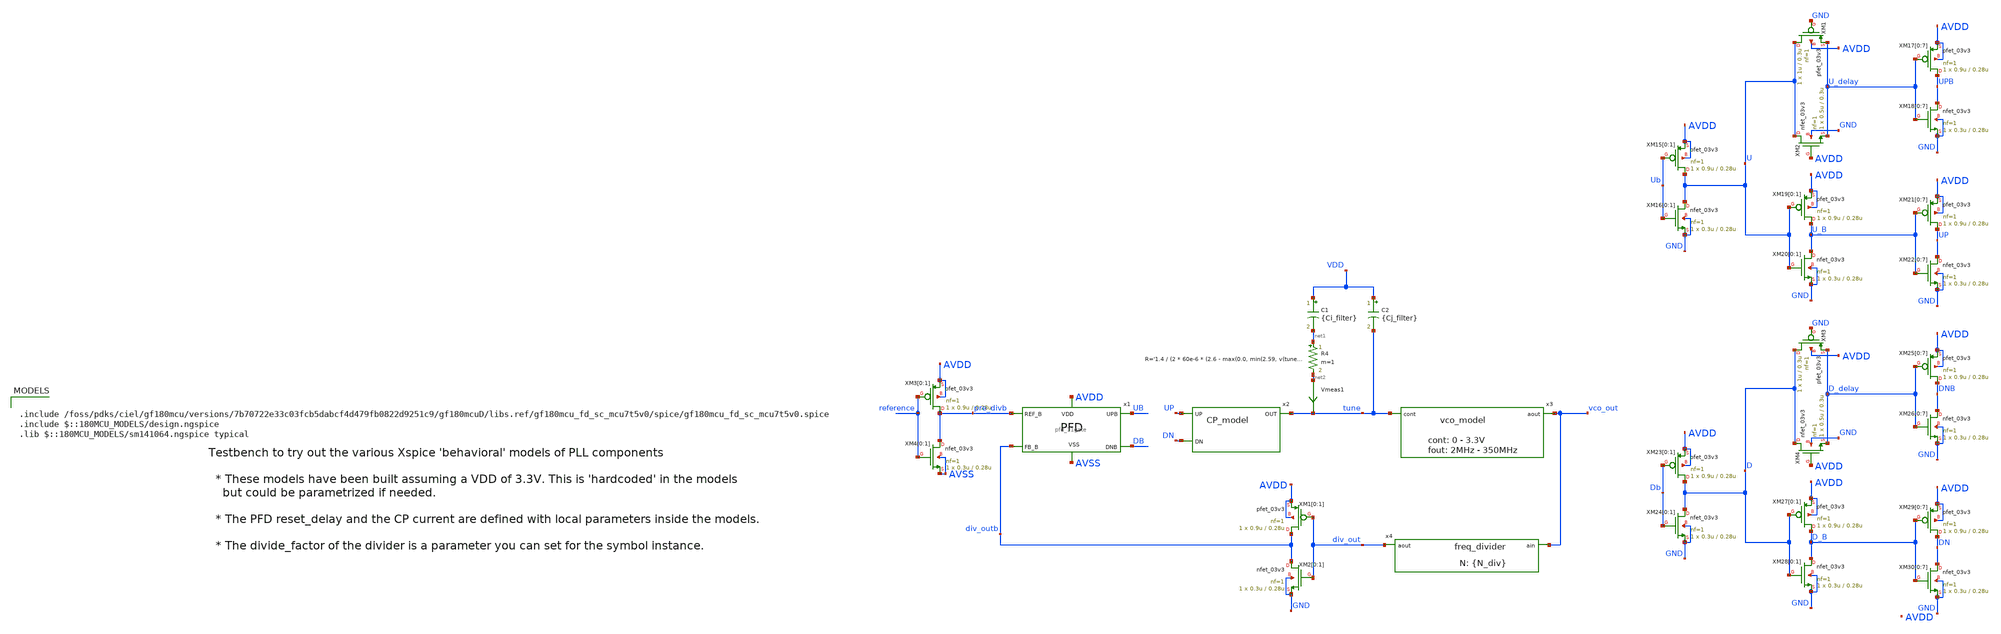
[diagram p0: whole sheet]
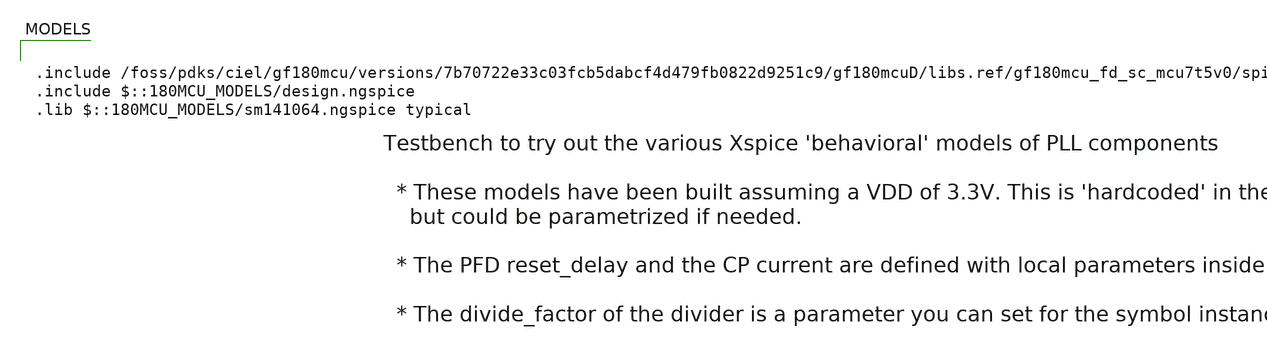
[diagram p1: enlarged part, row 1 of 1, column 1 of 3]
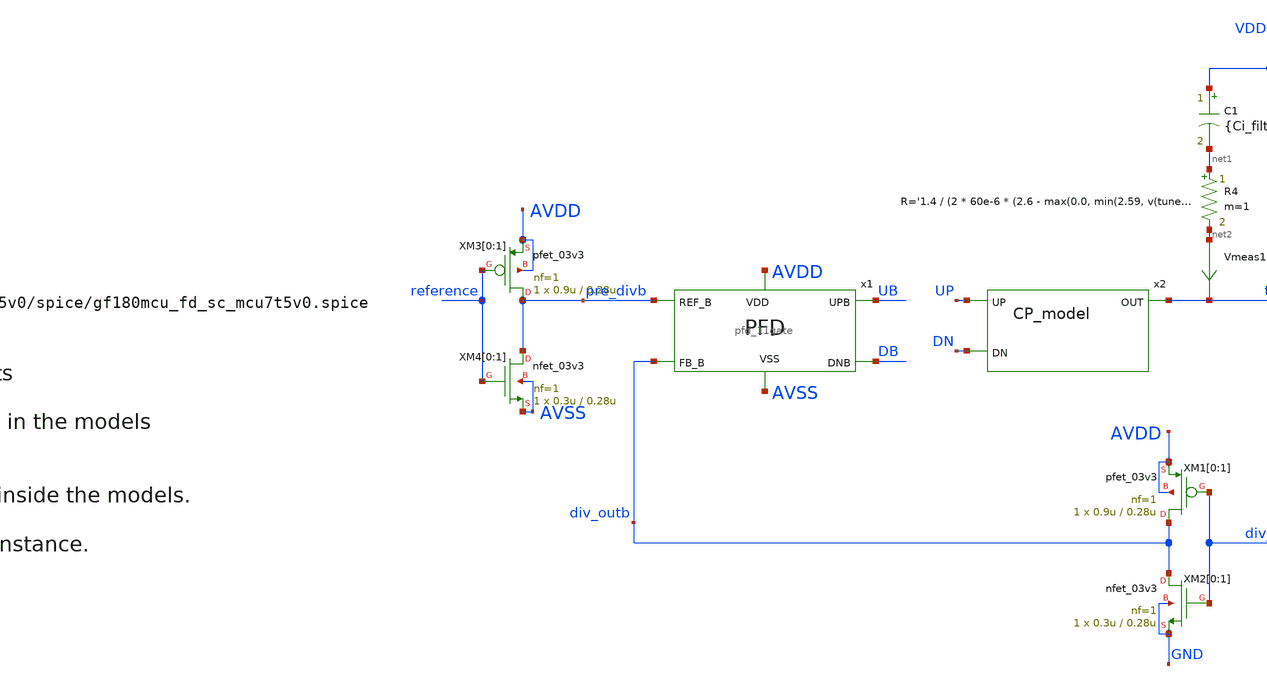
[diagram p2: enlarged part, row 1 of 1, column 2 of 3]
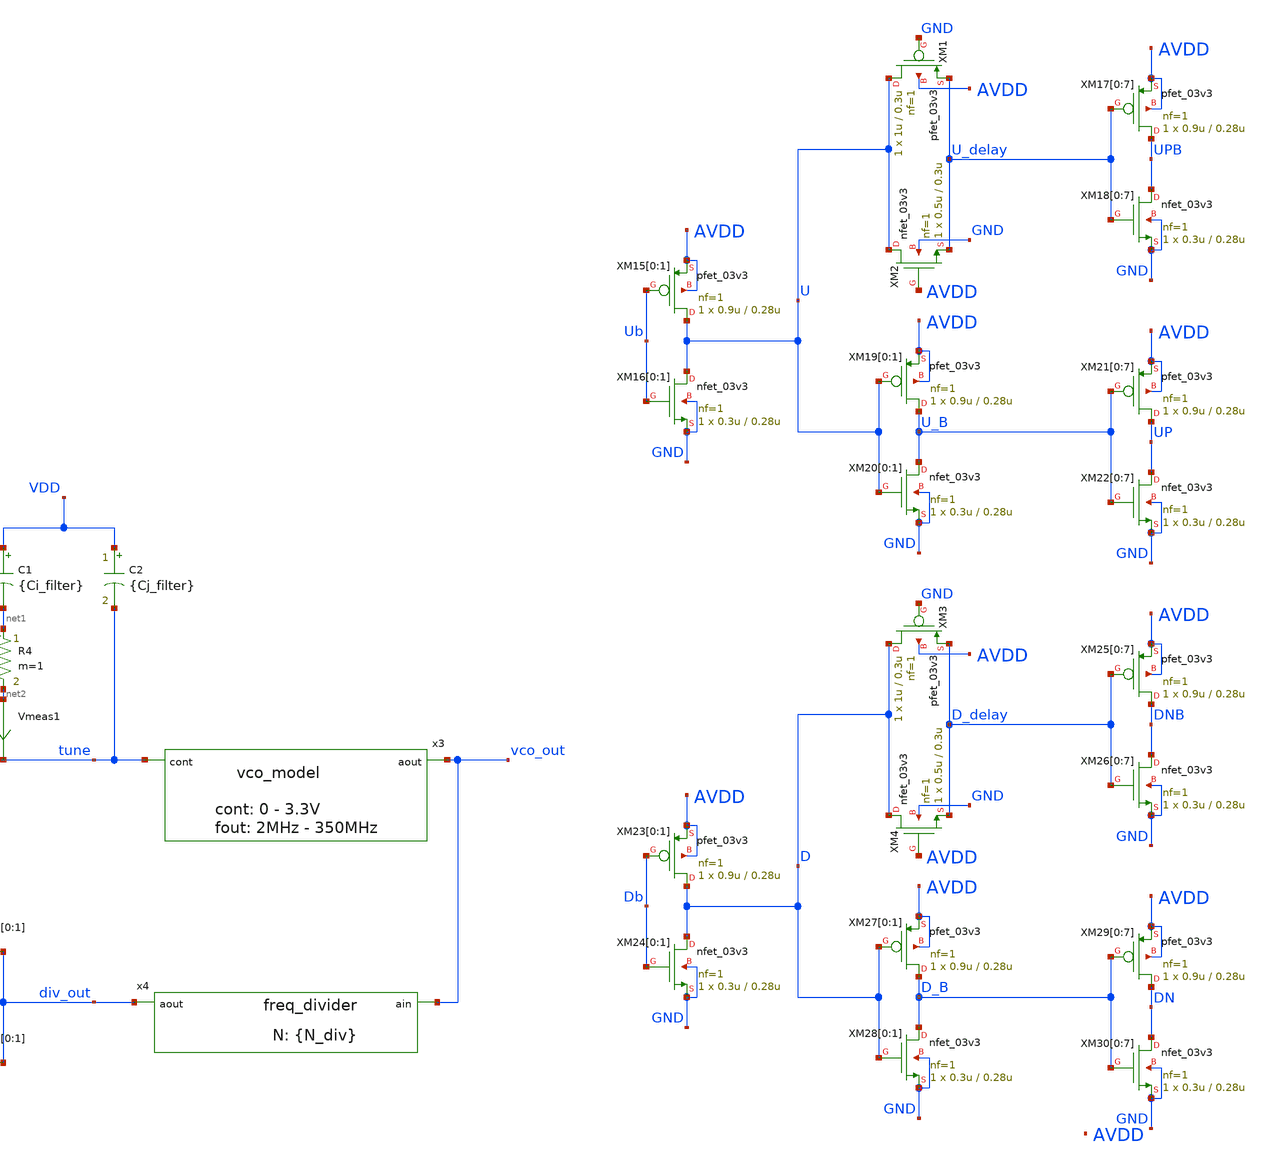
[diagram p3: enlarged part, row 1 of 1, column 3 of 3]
** sch_path: designs/libs/tb_pll/tb_PLL_PFD_model.sch
**.subckt tb_PLL_PFD_model
C1 VDD net1 {Ci_filter} m=1
R4 net1 net2 R='1.4 / (2 * 60e-6 * (2.6 - max(0.0, min(2.59, v(tune)))))' m=1
C2 VDD tune {Cj_filter} m=1
x2 tune UP DN CP_model
x3 vco_out tune vco_model
x4 div_out vco_out freq_divider divide_factor={N_div}
Vmeas1 net2 tune 0
.save i(vmeas1)
x1 pre_divb UB DB div_outb AVDD AVSS pfd_11gate
XM15[0] U Ub AVDD AVDD pfet_03v3 L=0.28u W=0.9u nf=1 ad='int((nf+1)/2) * W/nf * 0.18u' as='int((nf+2)/2) * W/nf * 0.18u'
+ pd='2*int((nf+1)/2) * (W/nf + 0.18u)' ps='2*int((nf+2)/2) * (W/nf + 0.18u)' nrd='0.18u / W' nrs='0.18u / W'
+ sa=0 sb=0 sd=0 m=1
XM15[1] U Ub AVDD AVDD pfet_03v3 L=0.28u W=0.9u nf=1 ad='int((nf+1)/2) * W/nf * 0.18u' as='int((nf+2)/2) * W/nf * 0.18u'
+ pd='2*int((nf+1)/2) * (W/nf + 0.18u)' ps='2*int((nf+2)/2) * (W/nf + 0.18u)' nrd='0.18u / W' nrs='0.18u / W'
+ sa=0 sb=0 sd=0 m=1
XM16[0] U Ub GND GND nfet_03v3 L=0.28u W=0.3u nf=1 ad='int((nf+1)/2) * W/nf * 0.18u' as='int((nf+2)/2) * W/nf * 0.18u'
+ pd='2*int((nf+1)/2) * (W/nf + 0.18u)' ps='2*int((nf+2)/2) * (W/nf + 0.18u)' nrd='0.18u / W' nrs='0.18u / W'
+ sa=0 sb=0 sd=0 m=1
XM16[1] U Ub GND GND nfet_03v3 L=0.28u W=0.3u nf=1 ad='int((nf+1)/2) * W/nf * 0.18u' as='int((nf+2)/2) * W/nf * 0.18u'
+ pd='2*int((nf+1)/2) * (W/nf + 0.18u)' ps='2*int((nf+2)/2) * (W/nf + 0.18u)' nrd='0.18u / W' nrs='0.18u / W'
+ sa=0 sb=0 sd=0 m=1
XM1 U GND U_delay AVDD pfet_03v3 L=0.3u W=1u nf=1 ad='int((nf+1)/2) * W/nf * 0.18u' as='int((nf+2)/2) * W/nf * 0.18u'
+ pd='2*int((nf+1)/2) * (W/nf + 0.18u)' ps='2*int((nf+2)/2) * (W/nf + 0.18u)' nrd='0.18u / W' nrs='0.18u / W'
+ sa=0 sb=0 sd=0 m=1
XM2 U AVDD U_delay GND nfet_03v3 L=0.3u W=0.5u nf=1 ad='int((nf+1)/2) * W/nf * 0.18u' as='int((nf+2)/2) * W/nf * 0.18u'
+ pd='2*int((nf+1)/2) * (W/nf + 0.18u)' ps='2*int((nf+2)/2) * (W/nf + 0.18u)' nrd='0.18u / W' nrs='0.18u / W'
+ sa=0 sb=0 sd=0 m=1
XM17[0] UPB U_delay AVDD AVDD pfet_03v3 L=0.28u W=0.9u nf=1 ad='int((nf+1)/2) * W/nf * 0.18u' as='int((nf+2)/2) * W/nf * 0.18u'
+ pd='2*int((nf+1)/2) * (W/nf + 0.18u)' ps='2*int((nf+2)/2) * (W/nf + 0.18u)' nrd='0.18u / W' nrs='0.18u / W'
+ sa=0 sb=0 sd=0 m=1
XM17[1] UPB U_delay AVDD AVDD pfet_03v3 L=0.28u W=0.9u nf=1 ad='int((nf+1)/2) * W/nf * 0.18u' as='int((nf+2)/2) * W/nf * 0.18u'
+ pd='2*int((nf+1)/2) * (W/nf + 0.18u)' ps='2*int((nf+2)/2) * (W/nf + 0.18u)' nrd='0.18u / W' nrs='0.18u / W'
+ sa=0 sb=0 sd=0 m=1
XM17[2] UPB U_delay AVDD AVDD pfet_03v3 L=0.28u W=0.9u nf=1 ad='int((nf+1)/2) * W/nf * 0.18u' as='int((nf+2)/2) * W/nf * 0.18u'
+ pd='2*int((nf+1)/2) * (W/nf + 0.18u)' ps='2*int((nf+2)/2) * (W/nf + 0.18u)' nrd='0.18u / W' nrs='0.18u / W'
+ sa=0 sb=0 sd=0 m=1
XM17[3] UPB U_delay AVDD AVDD pfet_03v3 L=0.28u W=0.9u nf=1 ad='int((nf+1)/2) * W/nf * 0.18u' as='int((nf+2)/2) * W/nf * 0.18u'
+ pd='2*int((nf+1)/2) * (W/nf + 0.18u)' ps='2*int((nf+2)/2) * (W/nf + 0.18u)' nrd='0.18u / W' nrs='0.18u / W'
+ sa=0 sb=0 sd=0 m=1
XM17[4] UPB U_delay AVDD AVDD pfet_03v3 L=0.28u W=0.9u nf=1 ad='int((nf+1)/2) * W/nf * 0.18u' as='int((nf+2)/2) * W/nf * 0.18u'
+ pd='2*int((nf+1)/2) * (W/nf + 0.18u)' ps='2*int((nf+2)/2) * (W/nf + 0.18u)' nrd='0.18u / W' nrs='0.18u / W'
+ sa=0 sb=0 sd=0 m=1
XM17[5] UPB U_delay AVDD AVDD pfet_03v3 L=0.28u W=0.9u nf=1 ad='int((nf+1)/2) * W/nf * 0.18u' as='int((nf+2)/2) * W/nf * 0.18u'
+ pd='2*int((nf+1)/2) * (W/nf + 0.18u)' ps='2*int((nf+2)/2) * (W/nf + 0.18u)' nrd='0.18u / W' nrs='0.18u / W'
+ sa=0 sb=0 sd=0 m=1
XM17[6] UPB U_delay AVDD AVDD pfet_03v3 L=0.28u W=0.9u nf=1 ad='int((nf+1)/2) * W/nf * 0.18u' as='int((nf+2)/2) * W/nf * 0.18u'
+ pd='2*int((nf+1)/2) * (W/nf + 0.18u)' ps='2*int((nf+2)/2) * (W/nf + 0.18u)' nrd='0.18u / W' nrs='0.18u / W'
+ sa=0 sb=0 sd=0 m=1
XM17[7] UPB U_delay AVDD AVDD pfet_03v3 L=0.28u W=0.9u nf=1 ad='int((nf+1)/2) * W/nf * 0.18u' as='int((nf+2)/2) * W/nf * 0.18u'
+ pd='2*int((nf+1)/2) * (W/nf + 0.18u)' ps='2*int((nf+2)/2) * (W/nf + 0.18u)' nrd='0.18u / W' nrs='0.18u / W'
+ sa=0 sb=0 sd=0 m=1
XM18[0] UPB U_delay GND GND nfet_03v3 L=0.28u W=0.3u nf=1 ad='int((nf+1)/2) * W/nf * 0.18u' as='int((nf+2)/2) * W/nf * 0.18u'
+ pd='2*int((nf+1)/2) * (W/nf + 0.18u)' ps='2*int((nf+2)/2) * (W/nf + 0.18u)' nrd='0.18u / W' nrs='0.18u / W'
+ sa=0 sb=0 sd=0 m=1
XM18[1] UPB U_delay GND GND nfet_03v3 L=0.28u W=0.3u nf=1 ad='int((nf+1)/2) * W/nf * 0.18u' as='int((nf+2)/2) * W/nf * 0.18u'
+ pd='2*int((nf+1)/2) * (W/nf + 0.18u)' ps='2*int((nf+2)/2) * (W/nf + 0.18u)' nrd='0.18u / W' nrs='0.18u / W'
+ sa=0 sb=0 sd=0 m=1
XM18[2] UPB U_delay GND GND nfet_03v3 L=0.28u W=0.3u nf=1 ad='int((nf+1)/2) * W/nf * 0.18u' as='int((nf+2)/2) * W/nf * 0.18u'
+ pd='2*int((nf+1)/2) * (W/nf + 0.18u)' ps='2*int((nf+2)/2) * (W/nf + 0.18u)' nrd='0.18u / W' nrs='0.18u / W'
+ sa=0 sb=0 sd=0 m=1
XM18[3] UPB U_delay GND GND nfet_03v3 L=0.28u W=0.3u nf=1 ad='int((nf+1)/2) * W/nf * 0.18u' as='int((nf+2)/2) * W/nf * 0.18u'
+ pd='2*int((nf+1)/2) * (W/nf + 0.18u)' ps='2*int((nf+2)/2) * (W/nf + 0.18u)' nrd='0.18u / W' nrs='0.18u / W'
+ sa=0 sb=0 sd=0 m=1
XM18[4] UPB U_delay GND GND nfet_03v3 L=0.28u W=0.3u nf=1 ad='int((nf+1)/2) * W/nf * 0.18u' as='int((nf+2)/2) * W/nf * 0.18u'
+ pd='2*int((nf+1)/2) * (W/nf + 0.18u)' ps='2*int((nf+2)/2) * (W/nf + 0.18u)' nrd='0.18u / W' nrs='0.18u / W'
+ sa=0 sb=0 sd=0 m=1
XM18[5] UPB U_delay GND GND nfet_03v3 L=0.28u W=0.3u nf=1 ad='int((nf+1)/2) * W/nf * 0.18u' as='int((nf+2)/2) * W/nf * 0.18u'
+ pd='2*int((nf+1)/2) * (W/nf + 0.18u)' ps='2*int((nf+2)/2) * (W/nf + 0.18u)' nrd='0.18u / W' nrs='0.18u / W'
+ sa=0 sb=0 sd=0 m=1
XM18[6] UPB U_delay GND GND nfet_03v3 L=0.28u W=0.3u nf=1 ad='int((nf+1)/2) * W/nf * 0.18u' as='int((nf+2)/2) * W/nf * 0.18u'
+ pd='2*int((nf+1)/2) * (W/nf + 0.18u)' ps='2*int((nf+2)/2) * (W/nf + 0.18u)' nrd='0.18u / W' nrs='0.18u / W'
+ sa=0 sb=0 sd=0 m=1
XM18[7] UPB U_delay GND GND nfet_03v3 L=0.28u W=0.3u nf=1 ad='int((nf+1)/2) * W/nf * 0.18u' as='int((nf+2)/2) * W/nf * 0.18u'
+ pd='2*int((nf+1)/2) * (W/nf + 0.18u)' ps='2*int((nf+2)/2) * (W/nf + 0.18u)' nrd='0.18u / W' nrs='0.18u / W'
+ sa=0 sb=0 sd=0 m=1
XM19[0] U_B U AVDD AVDD pfet_03v3 L=0.28u W=0.9u nf=1 ad='int((nf+1)/2) * W/nf * 0.18u' as='int((nf+2)/2) * W/nf * 0.18u'
+ pd='2*int((nf+1)/2) * (W/nf + 0.18u)' ps='2*int((nf+2)/2) * (W/nf + 0.18u)' nrd='0.18u / W' nrs='0.18u / W'
+ sa=0 sb=0 sd=0 m=1
XM19[1] U_B U AVDD AVDD pfet_03v3 L=0.28u W=0.9u nf=1 ad='int((nf+1)/2) * W/nf * 0.18u' as='int((nf+2)/2) * W/nf * 0.18u'
+ pd='2*int((nf+1)/2) * (W/nf + 0.18u)' ps='2*int((nf+2)/2) * (W/nf + 0.18u)' nrd='0.18u / W' nrs='0.18u / W'
+ sa=0 sb=0 sd=0 m=1
XM20[0] U_B U GND GND nfet_03v3 L=0.28u W=0.3u nf=1 ad='int((nf+1)/2) * W/nf * 0.18u' as='int((nf+2)/2) * W/nf * 0.18u'
+ pd='2*int((nf+1)/2) * (W/nf + 0.18u)' ps='2*int((nf+2)/2) * (W/nf + 0.18u)' nrd='0.18u / W' nrs='0.18u / W'
+ sa=0 sb=0 sd=0 m=1
XM20[1] U_B U GND GND nfet_03v3 L=0.28u W=0.3u nf=1 ad='int((nf+1)/2) * W/nf * 0.18u' as='int((nf+2)/2) * W/nf * 0.18u'
+ pd='2*int((nf+1)/2) * (W/nf + 0.18u)' ps='2*int((nf+2)/2) * (W/nf + 0.18u)' nrd='0.18u / W' nrs='0.18u / W'
+ sa=0 sb=0 sd=0 m=1
XM21[0] UP U_B AVDD AVDD pfet_03v3 L=0.28u W=0.9u nf=1 ad='int((nf+1)/2) * W/nf * 0.18u' as='int((nf+2)/2) * W/nf * 0.18u'
+ pd='2*int((nf+1)/2) * (W/nf + 0.18u)' ps='2*int((nf+2)/2) * (W/nf + 0.18u)' nrd='0.18u / W' nrs='0.18u / W'
+ sa=0 sb=0 sd=0 m=1
XM21[1] UP U_B AVDD AVDD pfet_03v3 L=0.28u W=0.9u nf=1 ad='int((nf+1)/2) * W/nf * 0.18u' as='int((nf+2)/2) * W/nf * 0.18u'
+ pd='2*int((nf+1)/2) * (W/nf + 0.18u)' ps='2*int((nf+2)/2) * (W/nf + 0.18u)' nrd='0.18u / W' nrs='0.18u / W'
+ sa=0 sb=0 sd=0 m=1
XM21[2] UP U_B AVDD AVDD pfet_03v3 L=0.28u W=0.9u nf=1 ad='int((nf+1)/2) * W/nf * 0.18u' as='int((nf+2)/2) * W/nf * 0.18u'
+ pd='2*int((nf+1)/2) * (W/nf + 0.18u)' ps='2*int((nf+2)/2) * (W/nf + 0.18u)' nrd='0.18u / W' nrs='0.18u / W'
+ sa=0 sb=0 sd=0 m=1
XM21[3] UP U_B AVDD AVDD pfet_03v3 L=0.28u W=0.9u nf=1 ad='int((nf+1)/2) * W/nf * 0.18u' as='int((nf+2)/2) * W/nf * 0.18u'
+ pd='2*int((nf+1)/2) * (W/nf + 0.18u)' ps='2*int((nf+2)/2) * (W/nf + 0.18u)' nrd='0.18u / W' nrs='0.18u / W'
+ sa=0 sb=0 sd=0 m=1
XM21[4] UP U_B AVDD AVDD pfet_03v3 L=0.28u W=0.9u nf=1 ad='int((nf+1)/2) * W/nf * 0.18u' as='int((nf+2)/2) * W/nf * 0.18u'
+ pd='2*int((nf+1)/2) * (W/nf + 0.18u)' ps='2*int((nf+2)/2) * (W/nf + 0.18u)' nrd='0.18u / W' nrs='0.18u / W'
+ sa=0 sb=0 sd=0 m=1
XM21[5] UP U_B AVDD AVDD pfet_03v3 L=0.28u W=0.9u nf=1 ad='int((nf+1)/2) * W/nf * 0.18u' as='int((nf+2)/2) * W/nf * 0.18u'
+ pd='2*int((nf+1)/2) * (W/nf + 0.18u)' ps='2*int((nf+2)/2) * (W/nf + 0.18u)' nrd='0.18u / W' nrs='0.18u / W'
+ sa=0 sb=0 sd=0 m=1
XM21[6] UP U_B AVDD AVDD pfet_03v3 L=0.28u W=0.9u nf=1 ad='int((nf+1)/2) * W/nf * 0.18u' as='int((nf+2)/2) * W/nf * 0.18u'
+ pd='2*int((nf+1)/2) * (W/nf + 0.18u)' ps='2*int((nf+2)/2) * (W/nf + 0.18u)' nrd='0.18u / W' nrs='0.18u / W'
+ sa=0 sb=0 sd=0 m=1
XM21[7] UP U_B AVDD AVDD pfet_03v3 L=0.28u W=0.9u nf=1 ad='int((nf+1)/2) * W/nf * 0.18u' as='int((nf+2)/2) * W/nf * 0.18u'
+ pd='2*int((nf+1)/2) * (W/nf + 0.18u)' ps='2*int((nf+2)/2) * (W/nf + 0.18u)' nrd='0.18u / W' nrs='0.18u / W'
+ sa=0 sb=0 sd=0 m=1
XM22[0] UP U_B GND GND nfet_03v3 L=0.28u W=0.3u nf=1 ad='int((nf+1)/2) * W/nf * 0.18u' as='int((nf+2)/2) * W/nf * 0.18u'
+ pd='2*int((nf+1)/2) * (W/nf + 0.18u)' ps='2*int((nf+2)/2) * (W/nf + 0.18u)' nrd='0.18u / W' nrs='0.18u / W'
+ sa=0 sb=0 sd=0 m=1
XM22[1] UP U_B GND GND nfet_03v3 L=0.28u W=0.3u nf=1 ad='int((nf+1)/2) * W/nf * 0.18u' as='int((nf+2)/2) * W/nf * 0.18u'
+ pd='2*int((nf+1)/2) * (W/nf + 0.18u)' ps='2*int((nf+2)/2) * (W/nf + 0.18u)' nrd='0.18u / W' nrs='0.18u / W'
+ sa=0 sb=0 sd=0 m=1
XM22[2] UP U_B GND GND nfet_03v3 L=0.28u W=0.3u nf=1 ad='int((nf+1)/2) * W/nf * 0.18u' as='int((nf+2)/2) * W/nf * 0.18u'
+ pd='2*int((nf+1)/2) * (W/nf + 0.18u)' ps='2*int((nf+2)/2) * (W/nf + 0.18u)' nrd='0.18u / W' nrs='0.18u / W'
+ sa=0 sb=0 sd=0 m=1
XM22[3] UP U_B GND GND nfet_03v3 L=0.28u W=0.3u nf=1 ad='int((nf+1)/2) * W/nf * 0.18u' as='int((nf+2)/2) * W/nf * 0.18u'
+ pd='2*int((nf+1)/2) * (W/nf + 0.18u)' ps='2*int((nf+2)/2) * (W/nf + 0.18u)' nrd='0.18u / W' nrs='0.18u / W'
+ sa=0 sb=0 sd=0 m=1
XM22[4] UP U_B GND GND nfet_03v3 L=0.28u W=0.3u nf=1 ad='int((nf+1)/2) * W/nf * 0.18u' as='int((nf+2)/2) * W/nf * 0.18u'
+ pd='2*int((nf+1)/2) * (W/nf + 0.18u)' ps='2*int((nf+2)/2) * (W/nf + 0.18u)' nrd='0.18u / W' nrs='0.18u / W'
+ sa=0 sb=0 sd=0 m=1
XM22[5] UP U_B GND GND nfet_03v3 L=0.28u W=0.3u nf=1 ad='int((nf+1)/2) * W/nf * 0.18u' as='int((nf+2)/2) * W/nf * 0.18u'
+ pd='2*int((nf+1)/2) * (W/nf + 0.18u)' ps='2*int((nf+2)/2) * (W/nf + 0.18u)' nrd='0.18u / W' nrs='0.18u / W'
+ sa=0 sb=0 sd=0 m=1
XM22[6] UP U_B GND GND nfet_03v3 L=0.28u W=0.3u nf=1 ad='int((nf+1)/2) * W/nf * 0.18u' as='int((nf+2)/2) * W/nf * 0.18u'
+ pd='2*int((nf+1)/2) * (W/nf + 0.18u)' ps='2*int((nf+2)/2) * (W/nf + 0.18u)' nrd='0.18u / W' nrs='0.18u / W'
+ sa=0 sb=0 sd=0 m=1
XM22[7] UP U_B GND GND nfet_03v3 L=0.28u W=0.3u nf=1 ad='int((nf+1)/2) * W/nf * 0.18u' as='int((nf+2)/2) * W/nf * 0.18u'
+ pd='2*int((nf+1)/2) * (W/nf + 0.18u)' ps='2*int((nf+2)/2) * (W/nf + 0.18u)' nrd='0.18u / W' nrs='0.18u / W'
+ sa=0 sb=0 sd=0 m=1
XM23[0] D Db AVDD AVDD pfet_03v3 L=0.28u W=0.9u nf=1 ad='int((nf+1)/2) * W/nf * 0.18u' as='int((nf+2)/2) * W/nf * 0.18u'
+ pd='2*int((nf+1)/2) * (W/nf + 0.18u)' ps='2*int((nf+2)/2) * (W/nf + 0.18u)' nrd='0.18u / W' nrs='0.18u / W'
+ sa=0 sb=0 sd=0 m=1
XM23[1] D Db AVDD AVDD pfet_03v3 L=0.28u W=0.9u nf=1 ad='int((nf+1)/2) * W/nf * 0.18u' as='int((nf+2)/2) * W/nf * 0.18u'
+ pd='2*int((nf+1)/2) * (W/nf + 0.18u)' ps='2*int((nf+2)/2) * (W/nf + 0.18u)' nrd='0.18u / W' nrs='0.18u / W'
+ sa=0 sb=0 sd=0 m=1
XM24[0] D Db GND GND nfet_03v3 L=0.28u W=0.3u nf=1 ad='int((nf+1)/2) * W/nf * 0.18u' as='int((nf+2)/2) * W/nf * 0.18u'
+ pd='2*int((nf+1)/2) * (W/nf + 0.18u)' ps='2*int((nf+2)/2) * (W/nf + 0.18u)' nrd='0.18u / W' nrs='0.18u / W'
+ sa=0 sb=0 sd=0 m=1
XM24[1] D Db GND GND nfet_03v3 L=0.28u W=0.3u nf=1 ad='int((nf+1)/2) * W/nf * 0.18u' as='int((nf+2)/2) * W/nf * 0.18u'
+ pd='2*int((nf+1)/2) * (W/nf + 0.18u)' ps='2*int((nf+2)/2) * (W/nf + 0.18u)' nrd='0.18u / W' nrs='0.18u / W'
+ sa=0 sb=0 sd=0 m=1
XM25[0] DNB D_delay AVDD AVDD pfet_03v3 L=0.28u W=0.9u nf=1 ad='int((nf+1)/2) * W/nf * 0.18u' as='int((nf+2)/2) * W/nf * 0.18u'
+ pd='2*int((nf+1)/2) * (W/nf + 0.18u)' ps='2*int((nf+2)/2) * (W/nf + 0.18u)' nrd='0.18u / W' nrs='0.18u / W'
+ sa=0 sb=0 sd=0 m=1
XM25[1] DNB D_delay AVDD AVDD pfet_03v3 L=0.28u W=0.9u nf=1 ad='int((nf+1)/2) * W/nf * 0.18u' as='int((nf+2)/2) * W/nf * 0.18u'
+ pd='2*int((nf+1)/2) * (W/nf + 0.18u)' ps='2*int((nf+2)/2) * (W/nf + 0.18u)' nrd='0.18u / W' nrs='0.18u / W'
+ sa=0 sb=0 sd=0 m=1
XM25[2] DNB D_delay AVDD AVDD pfet_03v3 L=0.28u W=0.9u nf=1 ad='int((nf+1)/2) * W/nf * 0.18u' as='int((nf+2)/2) * W/nf * 0.18u'
+ pd='2*int((nf+1)/2) * (W/nf + 0.18u)' ps='2*int((nf+2)/2) * (W/nf + 0.18u)' nrd='0.18u / W' nrs='0.18u / W'
+ sa=0 sb=0 sd=0 m=1
XM25[3] DNB D_delay AVDD AVDD pfet_03v3 L=0.28u W=0.9u nf=1 ad='int((nf+1)/2) * W/nf * 0.18u' as='int((nf+2)/2) * W/nf * 0.18u'
+ pd='2*int((nf+1)/2) * (W/nf + 0.18u)' ps='2*int((nf+2)/2) * (W/nf + 0.18u)' nrd='0.18u / W' nrs='0.18u / W'
+ sa=0 sb=0 sd=0 m=1
XM25[4] DNB D_delay AVDD AVDD pfet_03v3 L=0.28u W=0.9u nf=1 ad='int((nf+1)/2) * W/nf * 0.18u' as='int((nf+2)/2) * W/nf * 0.18u'
+ pd='2*int((nf+1)/2) * (W/nf + 0.18u)' ps='2*int((nf+2)/2) * (W/nf + 0.18u)' nrd='0.18u / W' nrs='0.18u / W'
+ sa=0 sb=0 sd=0 m=1
XM25[5] DNB D_delay AVDD AVDD pfet_03v3 L=0.28u W=0.9u nf=1 ad='int((nf+1)/2) * W/nf * 0.18u' as='int((nf+2)/2) * W/nf * 0.18u'
+ pd='2*int((nf+1)/2) * (W/nf + 0.18u)' ps='2*int((nf+2)/2) * (W/nf + 0.18u)' nrd='0.18u / W' nrs='0.18u / W'
+ sa=0 sb=0 sd=0 m=1
XM25[6] DNB D_delay AVDD AVDD pfet_03v3 L=0.28u W=0.9u nf=1 ad='int((nf+1)/2) * W/nf * 0.18u' as='int((nf+2)/2) * W/nf * 0.18u'
+ pd='2*int((nf+1)/2) * (W/nf + 0.18u)' ps='2*int((nf+2)/2) * (W/nf + 0.18u)' nrd='0.18u / W' nrs='0.18u / W'
+ sa=0 sb=0 sd=0 m=1
XM25[7] DNB D_delay AVDD AVDD pfet_03v3 L=0.28u W=0.9u nf=1 ad='int((nf+1)/2) * W/nf * 0.18u' as='int((nf+2)/2) * W/nf * 0.18u'
+ pd='2*int((nf+1)/2) * (W/nf + 0.18u)' ps='2*int((nf+2)/2) * (W/nf + 0.18u)' nrd='0.18u / W' nrs='0.18u / W'
+ sa=0 sb=0 sd=0 m=1
XM26[0] DNB D_delay GND GND nfet_03v3 L=0.28u W=0.3u nf=1 ad='int((nf+1)/2) * W/nf * 0.18u' as='int((nf+2)/2) * W/nf * 0.18u'
+ pd='2*int((nf+1)/2) * (W/nf + 0.18u)' ps='2*int((nf+2)/2) * (W/nf + 0.18u)' nrd='0.18u / W' nrs='0.18u / W'
+ sa=0 sb=0 sd=0 m=1
XM26[1] DNB D_delay GND GND nfet_03v3 L=0.28u W=0.3u nf=1 ad='int((nf+1)/2) * W/nf * 0.18u' as='int((nf+2)/2) * W/nf * 0.18u'
+ pd='2*int((nf+1)/2) * (W/nf + 0.18u)' ps='2*int((nf+2)/2) * (W/nf + 0.18u)' nrd='0.18u / W' nrs='0.18u / W'
+ sa=0 sb=0 sd=0 m=1
XM26[2] DNB D_delay GND GND nfet_03v3 L=0.28u W=0.3u nf=1 ad='int((nf+1)/2) * W/nf * 0.18u' as='int((nf+2)/2) * W/nf * 0.18u'
+ pd='2*int((nf+1)/2) * (W/nf + 0.18u)' ps='2*int((nf+2)/2) * (W/nf + 0.18u)' nrd='0.18u / W' nrs='0.18u / W'
+ sa=0 sb=0 sd=0 m=1
XM26[3] DNB D_delay GND GND nfet_03v3 L=0.28u W=0.3u nf=1 ad='int((nf+1)/2) * W/nf * 0.18u' as='int((nf+2)/2) * W/nf * 0.18u'
+ pd='2*int((nf+1)/2) * (W/nf + 0.18u)' ps='2*int((nf+2)/2) * (W/nf + 0.18u)' nrd='0.18u / W' nrs='0.18u / W'
+ sa=0 sb=0 sd=0 m=1
XM26[4] DNB D_delay GND GND nfet_03v3 L=0.28u W=0.3u nf=1 ad='int((nf+1)/2) * W/nf * 0.18u' as='int((nf+2)/2) * W/nf * 0.18u'
+ pd='2*int((nf+1)/2) * (W/nf + 0.18u)' ps='2*int((nf+2)/2) * (W/nf + 0.18u)' nrd='0.18u / W' nrs='0.18u / W'
+ sa=0 sb=0 sd=0 m=1
XM26[5] DNB D_delay GND GND nfet_03v3 L=0.28u W=0.3u nf=1 ad='int((nf+1)/2) * W/nf * 0.18u' as='int((nf+2)/2) * W/nf * 0.18u'
+ pd='2*int((nf+1)/2) * (W/nf + 0.18u)' ps='2*int((nf+2)/2) * (W/nf + 0.18u)' nrd='0.18u / W' nrs='0.18u / W'
+ sa=0 sb=0 sd=0 m=1
XM26[6] DNB D_delay GND GND nfet_03v3 L=0.28u W=0.3u nf=1 ad='int((nf+1)/2) * W/nf * 0.18u' as='int((nf+2)/2) * W/nf * 0.18u'
+ pd='2*int((nf+1)/2) * (W/nf + 0.18u)' ps='2*int((nf+2)/2) * (W/nf + 0.18u)' nrd='0.18u / W' nrs='0.18u / W'
+ sa=0 sb=0 sd=0 m=1
XM26[7] DNB D_delay GND GND nfet_03v3 L=0.28u W=0.3u nf=1 ad='int((nf+1)/2) * W/nf * 0.18u' as='int((nf+2)/2) * W/nf * 0.18u'
+ pd='2*int((nf+1)/2) * (W/nf + 0.18u)' ps='2*int((nf+2)/2) * (W/nf + 0.18u)' nrd='0.18u / W' nrs='0.18u / W'
+ sa=0 sb=0 sd=0 m=1
XM27[0] D_B D AVDD AVDD pfet_03v3 L=0.28u W=0.9u nf=1 ad='int((nf+1)/2) * W/nf * 0.18u' as='int((nf+2)/2) * W/nf * 0.18u'
+ pd='2*int((nf+1)/2) * (W/nf + 0.18u)' ps='2*int((nf+2)/2) * (W/nf + 0.18u)' nrd='0.18u / W' nrs='0.18u / W'
+ sa=0 sb=0 sd=0 m=1
XM27[1] D_B D AVDD AVDD pfet_03v3 L=0.28u W=0.9u nf=1 ad='int((nf+1)/2) * W/nf * 0.18u' as='int((nf+2)/2) * W/nf * 0.18u'
+ pd='2*int((nf+1)/2) * (W/nf + 0.18u)' ps='2*int((nf+2)/2) * (W/nf + 0.18u)' nrd='0.18u / W' nrs='0.18u / W'
+ sa=0 sb=0 sd=0 m=1
XM28[0] D_B D GND GND nfet_03v3 L=0.28u W=0.3u nf=1 ad='int((nf+1)/2) * W/nf * 0.18u' as='int((nf+2)/2) * W/nf * 0.18u'
+ pd='2*int((nf+1)/2) * (W/nf + 0.18u)' ps='2*int((nf+2)/2) * (W/nf + 0.18u)' nrd='0.18u / W' nrs='0.18u / W'
+ sa=0 sb=0 sd=0 m=1
XM28[1] D_B D GND GND nfet_03v3 L=0.28u W=0.3u nf=1 ad='int((nf+1)/2) * W/nf * 0.18u' as='int((nf+2)/2) * W/nf * 0.18u'
+ pd='2*int((nf+1)/2) * (W/nf + 0.18u)' ps='2*int((nf+2)/2) * (W/nf + 0.18u)' nrd='0.18u / W' nrs='0.18u / W'
+ sa=0 sb=0 sd=0 m=1
XM29[0] DN D_B AVDD AVDD pfet_03v3 L=0.28u W=0.9u nf=1 ad='int((nf+1)/2) * W/nf * 0.18u' as='int((nf+2)/2) * W/nf * 0.18u'
+ pd='2*int((nf+1)/2) * (W/nf + 0.18u)' ps='2*int((nf+2)/2) * (W/nf + 0.18u)' nrd='0.18u / W' nrs='0.18u / W'
+ sa=0 sb=0 sd=0 m=1
XM29[1] DN D_B AVDD AVDD pfet_03v3 L=0.28u W=0.9u nf=1 ad='int((nf+1)/2) * W/nf * 0.18u' as='int((nf+2)/2) * W/nf * 0.18u'
+ pd='2*int((nf+1)/2) * (W/nf + 0.18u)' ps='2*int((nf+2)/2) * (W/nf + 0.18u)' nrd='0.18u / W' nrs='0.18u / W'
+ sa=0 sb=0 sd=0 m=1
XM29[2] DN D_B AVDD AVDD pfet_03v3 L=0.28u W=0.9u nf=1 ad='int((nf+1)/2) * W/nf * 0.18u' as='int((nf+2)/2) * W/nf * 0.18u'
+ pd='2*int((nf+1)/2) * (W/nf + 0.18u)' ps='2*int((nf+2)/2) * (W/nf + 0.18u)' nrd='0.18u / W' nrs='0.18u / W'
+ sa=0 sb=0 sd=0 m=1
XM29[3] DN D_B AVDD AVDD pfet_03v3 L=0.28u W=0.9u nf=1 ad='int((nf+1)/2) * W/nf * 0.18u' as='int((nf+2)/2) * W/nf * 0.18u'
+ pd='2*int((nf+1)/2) * (W/nf + 0.18u)' ps='2*int((nf+2)/2) * (W/nf + 0.18u)' nrd='0.18u / W' nrs='0.18u / W'
+ sa=0 sb=0 sd=0 m=1
XM29[4] DN D_B AVDD AVDD pfet_03v3 L=0.28u W=0.9u nf=1 ad='int((nf+1)/2) * W/nf * 0.18u' as='int((nf+2)/2) * W/nf * 0.18u'
+ pd='2*int((nf+1)/2) * (W/nf + 0.18u)' ps='2*int((nf+2)/2) * (W/nf + 0.18u)' nrd='0.18u / W' nrs='0.18u / W'
+ sa=0 sb=0 sd=0 m=1
XM29[5] DN D_B AVDD AVDD pfet_03v3 L=0.28u W=0.9u nf=1 ad='int((nf+1)/2) * W/nf * 0.18u' as='int((nf+2)/2) * W/nf * 0.18u'
+ pd='2*int((nf+1)/2) * (W/nf + 0.18u)' ps='2*int((nf+2)/2) * (W/nf + 0.18u)' nrd='0.18u / W' nrs='0.18u / W'
+ sa=0 sb=0 sd=0 m=1
XM29[6] DN D_B AVDD AVDD pfet_03v3 L=0.28u W=0.9u nf=1 ad='int((nf+1)/2) * W/nf * 0.18u' as='int((nf+2)/2) * W/nf * 0.18u'
+ pd='2*int((nf+1)/2) * (W/nf + 0.18u)' ps='2*int((nf+2)/2) * (W/nf + 0.18u)' nrd='0.18u / W' nrs='0.18u / W'
+ sa=0 sb=0 sd=0 m=1
XM29[7] DN D_B AVDD AVDD pfet_03v3 L=0.28u W=0.9u nf=1 ad='int((nf+1)/2) * W/nf * 0.18u' as='int((nf+2)/2) * W/nf * 0.18u'
+ pd='2*int((nf+1)/2) * (W/nf + 0.18u)' ps='2*int((nf+2)/2) * (W/nf + 0.18u)' nrd='0.18u / W' nrs='0.18u / W'
+ sa=0 sb=0 sd=0 m=1
XM30[0] DN D_B GND GND nfet_03v3 L=0.28u W=0.3u nf=1 ad='int((nf+1)/2) * W/nf * 0.18u' as='int((nf+2)/2) * W/nf * 0.18u'
+ pd='2*int((nf+1)/2) * (W/nf + 0.18u)' ps='2*int((nf+2)/2) * (W/nf + 0.18u)' nrd='0.18u / W' nrs='0.18u / W'
+ sa=0 sb=0 sd=0 m=1
XM30[1] DN D_B GND GND nfet_03v3 L=0.28u W=0.3u nf=1 ad='int((nf+1)/2) * W/nf * 0.18u' as='int((nf+2)/2) * W/nf * 0.18u'
+ pd='2*int((nf+1)/2) * (W/nf + 0.18u)' ps='2*int((nf+2)/2) * (W/nf + 0.18u)' nrd='0.18u / W' nrs='0.18u / W'
+ sa=0 sb=0 sd=0 m=1
XM30[2] DN D_B GND GND nfet_03v3 L=0.28u W=0.3u nf=1 ad='int((nf+1)/2) * W/nf * 0.18u' as='int((nf+2)/2) * W/nf * 0.18u'
+ pd='2*int((nf+1)/2) * (W/nf + 0.18u)' ps='2*int((nf+2)/2) * (W/nf + 0.18u)' nrd='0.18u / W' nrs='0.18u / W'
+ sa=0 sb=0 sd=0 m=1
XM30[3] DN D_B GND GND nfet_03v3 L=0.28u W=0.3u nf=1 ad='int((nf+1)/2) * W/nf * 0.18u' as='int((nf+2)/2) * W/nf * 0.18u'
+ pd='2*int((nf+1)/2) * (W/nf + 0.18u)' ps='2*int((nf+2)/2) * (W/nf + 0.18u)' nrd='0.18u / W' nrs='0.18u / W'
+ sa=0 sb=0 sd=0 m=1
XM30[4] DN D_B GND GND nfet_03v3 L=0.28u W=0.3u nf=1 ad='int((nf+1)/2) * W/nf * 0.18u' as='int((nf+2)/2) * W/nf * 0.18u'
+ pd='2*int((nf+1)/2) * (W/nf + 0.18u)' ps='2*int((nf+2)/2) * (W/nf + 0.18u)' nrd='0.18u / W' nrs='0.18u / W'
+ sa=0 sb=0 sd=0 m=1
XM30[5] DN D_B GND GND nfet_03v3 L=0.28u W=0.3u nf=1 ad='int((nf+1)/2) * W/nf * 0.18u' as='int((nf+2)/2) * W/nf * 0.18u'
+ pd='2*int((nf+1)/2) * (W/nf + 0.18u)' ps='2*int((nf+2)/2) * (W/nf + 0.18u)' nrd='0.18u / W' nrs='0.18u / W'
+ sa=0 sb=0 sd=0 m=1
XM30[6] DN D_B GND GND nfet_03v3 L=0.28u W=0.3u nf=1 ad='int((nf+1)/2) * W/nf * 0.18u' as='int((nf+2)/2) * W/nf * 0.18u'
+ pd='2*int((nf+1)/2) * (W/nf + 0.18u)' ps='2*int((nf+2)/2) * (W/nf + 0.18u)' nrd='0.18u / W' nrs='0.18u / W'
+ sa=0 sb=0 sd=0 m=1
XM30[7] DN D_B GND GND nfet_03v3 L=0.28u W=0.3u nf=1 ad='int((nf+1)/2) * W/nf * 0.18u' as='int((nf+2)/2) * W/nf * 0.18u'
+ pd='2*int((nf+1)/2) * (W/nf + 0.18u)' ps='2*int((nf+2)/2) * (W/nf + 0.18u)' nrd='0.18u / W' nrs='0.18u / W'
+ sa=0 sb=0 sd=0 m=1
XM3 D GND D_delay AVDD pfet_03v3 L=0.3u W=1u nf=1 ad='int((nf+1)/2) * W/nf * 0.18u' as='int((nf+2)/2) * W/nf * 0.18u'
+ pd='2*int((nf+1)/2) * (W/nf + 0.18u)' ps='2*int((nf+2)/2) * (W/nf + 0.18u)' nrd='0.18u / W' nrs='0.18u / W'
+ sa=0 sb=0 sd=0 m=1
XM4 D AVDD D_delay GND nfet_03v3 L=0.3u W=0.5u nf=1 ad='int((nf+1)/2) * W/nf * 0.18u' as='int((nf+2)/2) * W/nf * 0.18u'
+ pd='2*int((nf+1)/2) * (W/nf + 0.18u)' ps='2*int((nf+2)/2) * (W/nf + 0.18u)' nrd='0.18u / W' nrs='0.18u / W'
+ sa=0 sb=0 sd=0 m=1
XM3[0] pre_divb reference AVDD AVDD pfet_03v3 L=0.28u W=0.9u nf=1 ad='int((nf+1)/2) * W/nf * 0.18u' as='int((nf+2)/2) * W/nf * 0.18u'
+ pd='2*int((nf+1)/2) * (W/nf + 0.18u)' ps='2*int((nf+2)/2) * (W/nf + 0.18u)' nrd='0.18u / W' nrs='0.18u / W'
+ sa=0 sb=0 sd=0 m=1
XM3[1] pre_divb reference AVDD AVDD pfet_03v3 L=0.28u W=0.9u nf=1 ad='int((nf+1)/2) * W/nf * 0.18u' as='int((nf+2)/2) * W/nf * 0.18u'
+ pd='2*int((nf+1)/2) * (W/nf + 0.18u)' ps='2*int((nf+2)/2) * (W/nf + 0.18u)' nrd='0.18u / W' nrs='0.18u / W'
+ sa=0 sb=0 sd=0 m=1
XM4[0] pre_divb reference AVSS AVSS nfet_03v3 L=0.28u W=0.3u nf=1 ad='int((nf+1)/2) * W/nf * 0.18u' as='int((nf+2)/2) * W/nf * 0.18u'
+ pd='2*int((nf+1)/2) * (W/nf + 0.18u)' ps='2*int((nf+2)/2) * (W/nf + 0.18u)' nrd='0.18u / W' nrs='0.18u / W'
+ sa=0 sb=0 sd=0 m=1
XM4[1] pre_divb reference AVSS AVSS nfet_03v3 L=0.28u W=0.3u nf=1 ad='int((nf+1)/2) * W/nf * 0.18u' as='int((nf+2)/2) * W/nf * 0.18u'
+ pd='2*int((nf+1)/2) * (W/nf + 0.18u)' ps='2*int((nf+2)/2) * (W/nf + 0.18u)' nrd='0.18u / W' nrs='0.18u / W'
+ sa=0 sb=0 sd=0 m=1
XM1[0] div_outb div_out AVDD AVDD pfet_03v3 L=0.28u W=0.9u nf=1 ad='int((nf+1)/2) * W/nf * 0.18u' as='int((nf+2)/2) * W/nf * 0.18u'
+ pd='2*int((nf+1)/2) * (W/nf + 0.18u)' ps='2*int((nf+2)/2) * (W/nf + 0.18u)' nrd='0.18u / W' nrs='0.18u / W'
+ sa=0 sb=0 sd=0 m=1
XM1[1] div_outb div_out AVDD AVDD pfet_03v3 L=0.28u W=0.9u nf=1 ad='int((nf+1)/2) * W/nf * 0.18u' as='int((nf+2)/2) * W/nf * 0.18u'
+ pd='2*int((nf+1)/2) * (W/nf + 0.18u)' ps='2*int((nf+2)/2) * (W/nf + 0.18u)' nrd='0.18u / W' nrs='0.18u / W'
+ sa=0 sb=0 sd=0 m=1
XM2[0] div_outb div_out GND GND nfet_03v3 L=0.28u W=0.3u nf=1 ad='int((nf+1)/2) * W/nf * 0.18u' as='int((nf+2)/2) * W/nf * 0.18u'
+ pd='2*int((nf+1)/2) * (W/nf + 0.18u)' ps='2*int((nf+2)/2) * (W/nf + 0.18u)' nrd='0.18u / W' nrs='0.18u / W'
+ sa=0 sb=0 sd=0 m=1
XM2[1] div_outb div_out GND GND nfet_03v3 L=0.28u W=0.3u nf=1 ad='int((nf+1)/2) * W/nf * 0.18u' as='int((nf+2)/2) * W/nf * 0.18u'
+ pd='2*int((nf+1)/2) * (W/nf + 0.18u)' ps='2*int((nf+2)/2) * (W/nf + 0.18u)' nrd='0.18u / W' nrs='0.18u / W'
+ sa=0 sb=0 sd=0 m=1
**** begin user architecture code

.include /foss/pdks/ciel/gf180mcu/versions/7b70722e33c03fcb5dabcf4d479fb0822d9251c9/gf180mcuD/libs.ref/gf180mcu_fd_sc_mcu7t5v0/spice/gf180mcu_fd_sc_mcu7t5v0.spice
.include $::180MCU_MODELS/design.ngspice
.lib $::180MCU_MODELS/sm141064.ngspice typical



.options method=gear
VDD VDD 0 3.3
VSS VSS 0 0
VAVDD AVDD 0 3.3
VAVSS AVSS 0 0
* control is for tests when opening the loop
* see the Vcontrol voltage source
.ic v(tune)=2
* reference frequency
.param f_ref = 1MEG
* divider
.param R_div=2
.param N_div=10
* loop filter parameters
.param Ci_filter = 10p
.param Cj_filter = 1p
.param td_ref='1/f_ref' tp_ref='td_ref/2'
Vref reference gnd pulse(0 3.3 0 10p 10p tp_ref td_ref)

.control
set wr_singlescale
set wr_vecnames

*save all
save v(vco_out) v(reference) v(up) v(dn) v(tune) v(pre_divb) v(div_out)  v(div_outb)
TRAN 10n 200u
remzerovec

write tb_PLL_PFD_model.raw
*wrdata /foss/designs/synchronos-chipathon-2026/designs/libs/scripts/sim_data/tb_PLL_div_model.txt
*+ tran.all
.endc


**** end user architecture code
**.ends
.end
